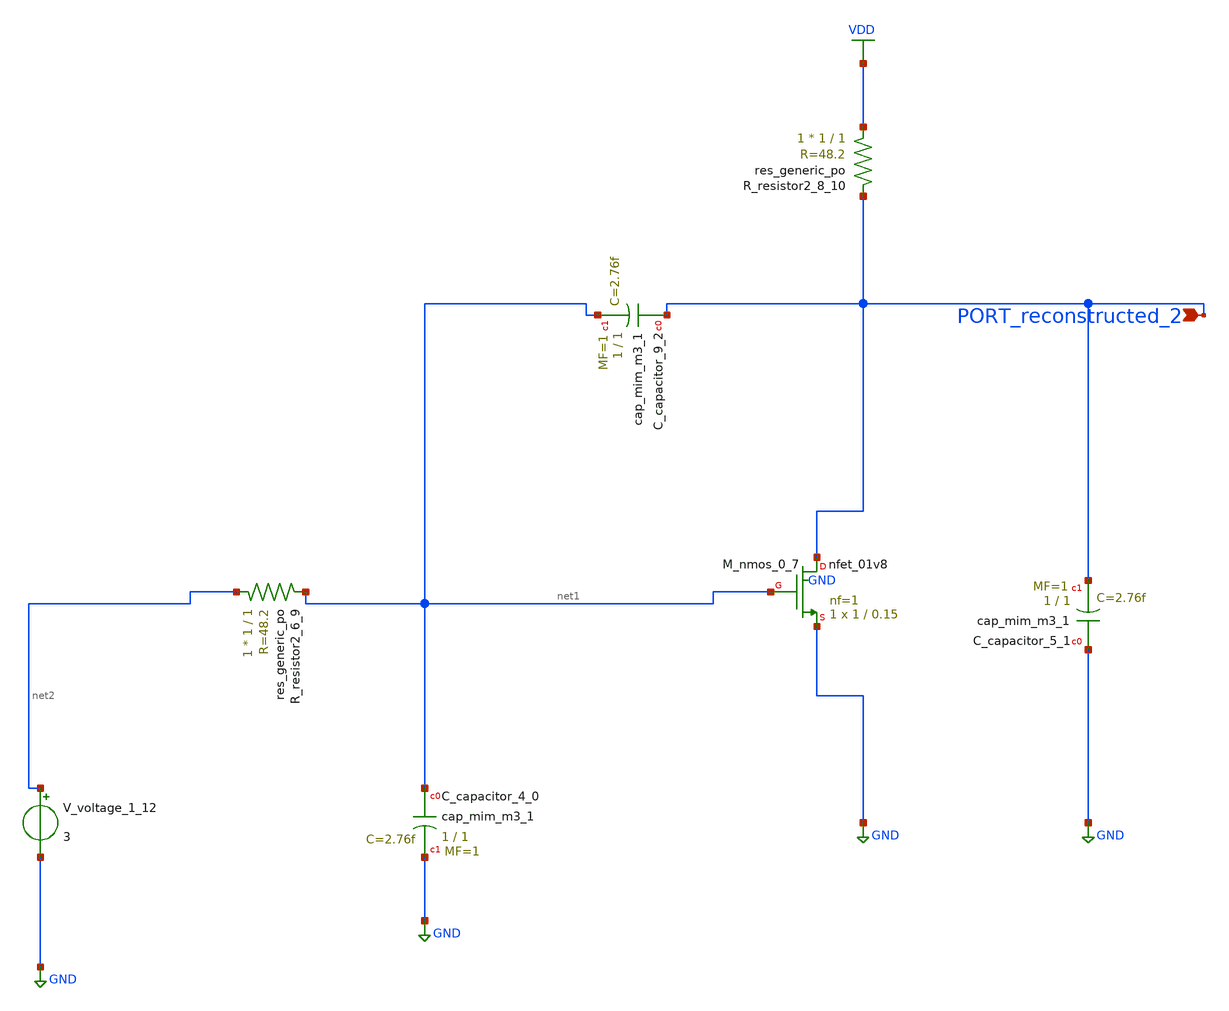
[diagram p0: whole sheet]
** sch_path: schematics/AMSNet/361.sch
**.subckt 361 PORT_reconstructed_2
*.ipin PORT_reconstructed_2
XC_capacitor_4_0 net1 GND sky130_fd_pr__cap_mim_m3_1 W=1 L=1 MF=1 m=1
XC_capacitor_5_1 GND PORT_reconstructed_2 sky130_fd_pr__cap_mim_m3_1 W=1 L=1 MF=1 m=1
XC_capacitor_9_2 PORT_reconstructed_2 net1 sky130_fd_pr__cap_mim_m3_1 W=1 L=1 MF=1 m=1
XM_nmos_0_7 PORT_reconstructed_2 net1 GND GND sky130_fd_pr__nfet_01v8 L=0.15 W=1 nf=1 ad='int((1 + 1)/2) * 1 / 1 * 0.29'
+ as='int((1 + 2)/2) * 1 / 1 * 0.29' pd='2*int((1 + 1)/2) * (1 / 1 + 0.29)' ps='2*int((1 + 2)/2) * (1 / 1 + 0.29)'
+ nrd='0.29 / 1 ' nrs='0.29 / 1 ' sa=0 sb=0 sd=0 mult=1 m=1
XR_resistor2_6_9 net2 net1 sky130_fd_pr__res_generic_po W=1 L=1 m=1
XR_resistor2_8_10 VDD PORT_reconstructed_2 sky130_fd_pr__res_generic_po W=1 L=1 m=1
V_voltage_1_12 net2 GND 3
**.ends
.GLOBAL GND
.GLOBAL VDD
.end
